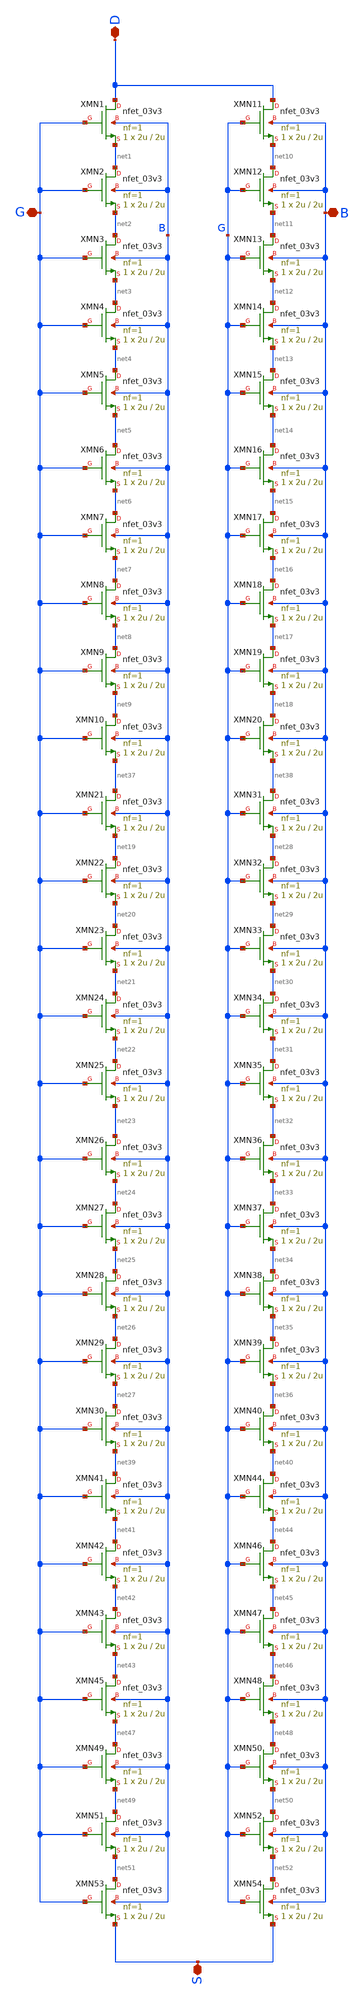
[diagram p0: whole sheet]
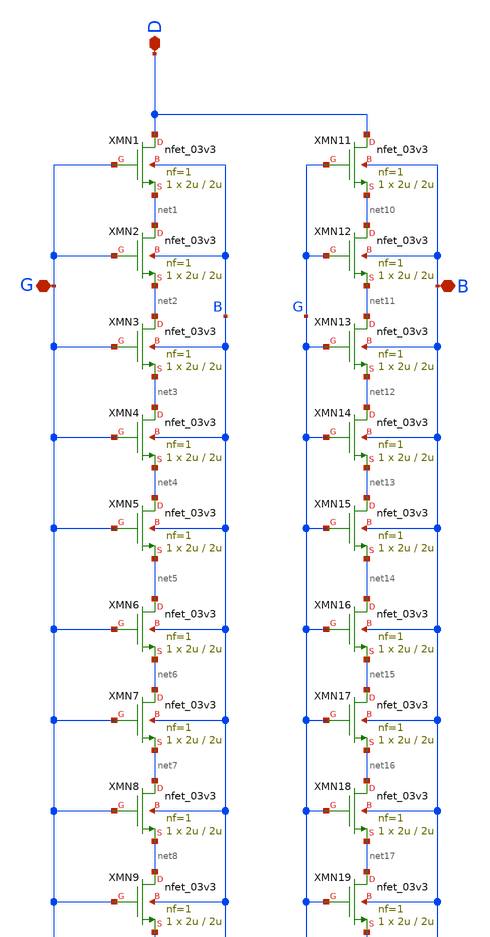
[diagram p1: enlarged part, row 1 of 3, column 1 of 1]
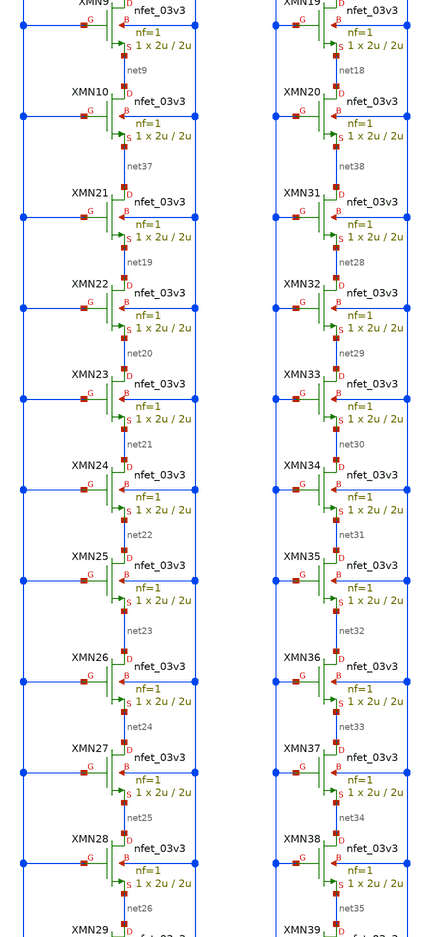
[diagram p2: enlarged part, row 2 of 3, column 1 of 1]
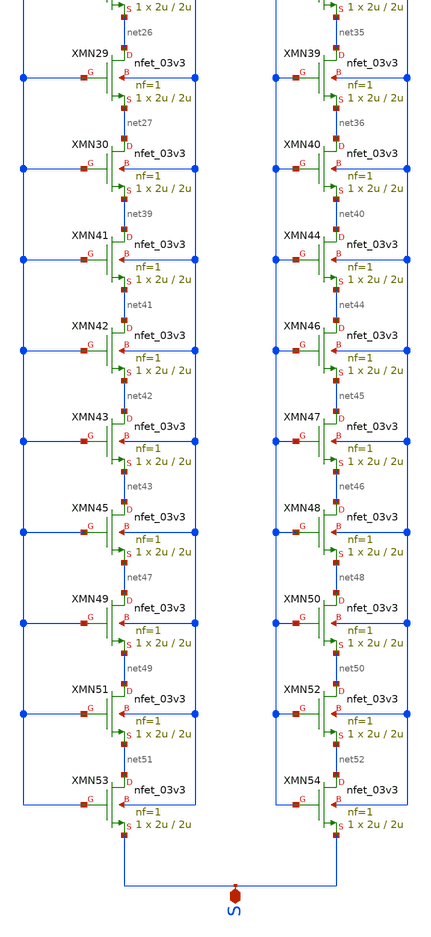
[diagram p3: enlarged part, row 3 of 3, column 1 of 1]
** sch_path: Voltage_Reference/symbols_vr/NMOS_matrix2_SCM1.sch
**.subckt NMOS_matrix2_SCM1 D G B S
*.iopin D
*.iopin G
*.iopin B
*.iopin S
XMN1 D G net1 B nfet_03v3 L=2u W=2u nf=1 ad='int((nf+1)/2) * W/nf * 0.18u' as='int((nf+2)/2) * W/nf * 0.18u'
+ pd='2*int((nf+1)/2) * (W/nf + 0.18u)' ps='2*int((nf+2)/2) * (W/nf + 0.18u)' nrd='0.18u / W' nrs='0.18u / W'
+ sa=0 sb=0 sd=0 m=1
XMN2 net1 G net2 B nfet_03v3 L=2u W=2u nf=1 ad='int((nf+1)/2) * W/nf * 0.18u' as='int((nf+2)/2) * W/nf * 0.18u'
+ pd='2*int((nf+1)/2) * (W/nf + 0.18u)' ps='2*int((nf+2)/2) * (W/nf + 0.18u)' nrd='0.18u / W' nrs='0.18u / W'
+ sa=0 sb=0 sd=0 m=1
XMN3 net2 G net3 B nfet_03v3 L=2u W=2u nf=1 ad='int((nf+1)/2) * W/nf * 0.18u' as='int((nf+2)/2) * W/nf * 0.18u'
+ pd='2*int((nf+1)/2) * (W/nf + 0.18u)' ps='2*int((nf+2)/2) * (W/nf + 0.18u)' nrd='0.18u / W' nrs='0.18u / W'
+ sa=0 sb=0 sd=0 m=1
XMN4 net3 G net4 B nfet_03v3 L=2u W=2u nf=1 ad='int((nf+1)/2) * W/nf * 0.18u' as='int((nf+2)/2) * W/nf * 0.18u'
+ pd='2*int((nf+1)/2) * (W/nf + 0.18u)' ps='2*int((nf+2)/2) * (W/nf + 0.18u)' nrd='0.18u / W' nrs='0.18u / W'
+ sa=0 sb=0 sd=0 m=1
XMN5 net4 G net5 B nfet_03v3 L=2u W=2u nf=1 ad='int((nf+1)/2) * W/nf * 0.18u' as='int((nf+2)/2) * W/nf * 0.18u'
+ pd='2*int((nf+1)/2) * (W/nf + 0.18u)' ps='2*int((nf+2)/2) * (W/nf + 0.18u)' nrd='0.18u / W' nrs='0.18u / W'
+ sa=0 sb=0 sd=0 m=1
XMN6 net5 G net6 B nfet_03v3 L=2u W=2u nf=1 ad='int((nf+1)/2) * W/nf * 0.18u' as='int((nf+2)/2) * W/nf * 0.18u'
+ pd='2*int((nf+1)/2) * (W/nf + 0.18u)' ps='2*int((nf+2)/2) * (W/nf + 0.18u)' nrd='0.18u / W' nrs='0.18u / W'
+ sa=0 sb=0 sd=0 m=1
XMN7 net6 G net7 B nfet_03v3 L=2u W=2u nf=1 ad='int((nf+1)/2) * W/nf * 0.18u' as='int((nf+2)/2) * W/nf * 0.18u'
+ pd='2*int((nf+1)/2) * (W/nf + 0.18u)' ps='2*int((nf+2)/2) * (W/nf + 0.18u)' nrd='0.18u / W' nrs='0.18u / W'
+ sa=0 sb=0 sd=0 m=1
XMN8 net7 G net8 B nfet_03v3 L=2u W=2u nf=1 ad='int((nf+1)/2) * W/nf * 0.18u' as='int((nf+2)/2) * W/nf * 0.18u'
+ pd='2*int((nf+1)/2) * (W/nf + 0.18u)' ps='2*int((nf+2)/2) * (W/nf + 0.18u)' nrd='0.18u / W' nrs='0.18u / W'
+ sa=0 sb=0 sd=0 m=1
XMN9 net8 G net9 B nfet_03v3 L=2u W=2u nf=1 ad='int((nf+1)/2) * W/nf * 0.18u' as='int((nf+2)/2) * W/nf * 0.18u'
+ pd='2*int((nf+1)/2) * (W/nf + 0.18u)' ps='2*int((nf+2)/2) * (W/nf + 0.18u)' nrd='0.18u / W' nrs='0.18u / W'
+ sa=0 sb=0 sd=0 m=1
XMN10 net9 G net37 B nfet_03v3 L=2u W=2u nf=1 ad='int((nf+1)/2) * W/nf * 0.18u' as='int((nf+2)/2) * W/nf * 0.18u'
+ pd='2*int((nf+1)/2) * (W/nf + 0.18u)' ps='2*int((nf+2)/2) * (W/nf + 0.18u)' nrd='0.18u / W' nrs='0.18u / W'
+ sa=0 sb=0 sd=0 m=1
XMN11 D G net10 B nfet_03v3 L=2u W=2u nf=1 ad='int((nf+1)/2) * W/nf * 0.18u' as='int((nf+2)/2) * W/nf * 0.18u'
+ pd='2*int((nf+1)/2) * (W/nf + 0.18u)' ps='2*int((nf+2)/2) * (W/nf + 0.18u)' nrd='0.18u / W' nrs='0.18u / W'
+ sa=0 sb=0 sd=0 m=1
XMN12 net10 G net11 B nfet_03v3 L=2u W=2u nf=1 ad='int((nf+1)/2) * W/nf * 0.18u' as='int((nf+2)/2) * W/nf * 0.18u'
+ pd='2*int((nf+1)/2) * (W/nf + 0.18u)' ps='2*int((nf+2)/2) * (W/nf + 0.18u)' nrd='0.18u / W' nrs='0.18u / W'
+ sa=0 sb=0 sd=0 m=1
XMN13 net11 G net12 B nfet_03v3 L=2u W=2u nf=1 ad='int((nf+1)/2) * W/nf * 0.18u' as='int((nf+2)/2) * W/nf * 0.18u'
+ pd='2*int((nf+1)/2) * (W/nf + 0.18u)' ps='2*int((nf+2)/2) * (W/nf + 0.18u)' nrd='0.18u / W' nrs='0.18u / W'
+ sa=0 sb=0 sd=0 m=1
XMN14 net12 G net13 B nfet_03v3 L=2u W=2u nf=1 ad='int((nf+1)/2) * W/nf * 0.18u' as='int((nf+2)/2) * W/nf * 0.18u'
+ pd='2*int((nf+1)/2) * (W/nf + 0.18u)' ps='2*int((nf+2)/2) * (W/nf + 0.18u)' nrd='0.18u / W' nrs='0.18u / W'
+ sa=0 sb=0 sd=0 m=1
XMN15 net13 G net14 B nfet_03v3 L=2u W=2u nf=1 ad='int((nf+1)/2) * W/nf * 0.18u' as='int((nf+2)/2) * W/nf * 0.18u'
+ pd='2*int((nf+1)/2) * (W/nf + 0.18u)' ps='2*int((nf+2)/2) * (W/nf + 0.18u)' nrd='0.18u / W' nrs='0.18u / W'
+ sa=0 sb=0 sd=0 m=1
XMN16 net14 G net15 B nfet_03v3 L=2u W=2u nf=1 ad='int((nf+1)/2) * W/nf * 0.18u' as='int((nf+2)/2) * W/nf * 0.18u'
+ pd='2*int((nf+1)/2) * (W/nf + 0.18u)' ps='2*int((nf+2)/2) * (W/nf + 0.18u)' nrd='0.18u / W' nrs='0.18u / W'
+ sa=0 sb=0 sd=0 m=1
XMN17 net15 G net16 B nfet_03v3 L=2u W=2u nf=1 ad='int((nf+1)/2) * W/nf * 0.18u' as='int((nf+2)/2) * W/nf * 0.18u'
+ pd='2*int((nf+1)/2) * (W/nf + 0.18u)' ps='2*int((nf+2)/2) * (W/nf + 0.18u)' nrd='0.18u / W' nrs='0.18u / W'
+ sa=0 sb=0 sd=0 m=1
XMN18 net16 G net17 B nfet_03v3 L=2u W=2u nf=1 ad='int((nf+1)/2) * W/nf * 0.18u' as='int((nf+2)/2) * W/nf * 0.18u'
+ pd='2*int((nf+1)/2) * (W/nf + 0.18u)' ps='2*int((nf+2)/2) * (W/nf + 0.18u)' nrd='0.18u / W' nrs='0.18u / W'
+ sa=0 sb=0 sd=0 m=1
XMN19 net17 G net18 B nfet_03v3 L=2u W=2u nf=1 ad='int((nf+1)/2) * W/nf * 0.18u' as='int((nf+2)/2) * W/nf * 0.18u'
+ pd='2*int((nf+1)/2) * (W/nf + 0.18u)' ps='2*int((nf+2)/2) * (W/nf + 0.18u)' nrd='0.18u / W' nrs='0.18u / W'
+ sa=0 sb=0 sd=0 m=1
XMN20 net18 G net38 B nfet_03v3 L=2u W=2u nf=1 ad='int((nf+1)/2) * W/nf * 0.18u' as='int((nf+2)/2) * W/nf * 0.18u'
+ pd='2*int((nf+1)/2) * (W/nf + 0.18u)' ps='2*int((nf+2)/2) * (W/nf + 0.18u)' nrd='0.18u / W' nrs='0.18u / W'
+ sa=0 sb=0 sd=0 m=1
XMN21 net37 G net19 B nfet_03v3 L=2u W=2u nf=1 ad='int((nf+1)/2) * W/nf * 0.18u' as='int((nf+2)/2) * W/nf * 0.18u'
+ pd='2*int((nf+1)/2) * (W/nf + 0.18u)' ps='2*int((nf+2)/2) * (W/nf + 0.18u)' nrd='0.18u / W' nrs='0.18u / W'
+ sa=0 sb=0 sd=0 m=1
XMN22 net19 G net20 B nfet_03v3 L=2u W=2u nf=1 ad='int((nf+1)/2) * W/nf * 0.18u' as='int((nf+2)/2) * W/nf * 0.18u'
+ pd='2*int((nf+1)/2) * (W/nf + 0.18u)' ps='2*int((nf+2)/2) * (W/nf + 0.18u)' nrd='0.18u / W' nrs='0.18u / W'
+ sa=0 sb=0 sd=0 m=1
XMN23 net20 G net21 B nfet_03v3 L=2u W=2u nf=1 ad='int((nf+1)/2) * W/nf * 0.18u' as='int((nf+2)/2) * W/nf * 0.18u'
+ pd='2*int((nf+1)/2) * (W/nf + 0.18u)' ps='2*int((nf+2)/2) * (W/nf + 0.18u)' nrd='0.18u / W' nrs='0.18u / W'
+ sa=0 sb=0 sd=0 m=1
XMN24 net21 G net22 B nfet_03v3 L=2u W=2u nf=1 ad='int((nf+1)/2) * W/nf * 0.18u' as='int((nf+2)/2) * W/nf * 0.18u'
+ pd='2*int((nf+1)/2) * (W/nf + 0.18u)' ps='2*int((nf+2)/2) * (W/nf + 0.18u)' nrd='0.18u / W' nrs='0.18u / W'
+ sa=0 sb=0 sd=0 m=1
XMN25 net22 G net23 B nfet_03v3 L=2u W=2u nf=1 ad='int((nf+1)/2) * W/nf * 0.18u' as='int((nf+2)/2) * W/nf * 0.18u'
+ pd='2*int((nf+1)/2) * (W/nf + 0.18u)' ps='2*int((nf+2)/2) * (W/nf + 0.18u)' nrd='0.18u / W' nrs='0.18u / W'
+ sa=0 sb=0 sd=0 m=1
XMN26 net23 G net24 B nfet_03v3 L=2u W=2u nf=1 ad='int((nf+1)/2) * W/nf * 0.18u' as='int((nf+2)/2) * W/nf * 0.18u'
+ pd='2*int((nf+1)/2) * (W/nf + 0.18u)' ps='2*int((nf+2)/2) * (W/nf + 0.18u)' nrd='0.18u / W' nrs='0.18u / W'
+ sa=0 sb=0 sd=0 m=1
XMN27 net24 G net25 B nfet_03v3 L=2u W=2u nf=1 ad='int((nf+1)/2) * W/nf * 0.18u' as='int((nf+2)/2) * W/nf * 0.18u'
+ pd='2*int((nf+1)/2) * (W/nf + 0.18u)' ps='2*int((nf+2)/2) * (W/nf + 0.18u)' nrd='0.18u / W' nrs='0.18u / W'
+ sa=0 sb=0 sd=0 m=1
XMN28 net25 G net26 B nfet_03v3 L=2u W=2u nf=1 ad='int((nf+1)/2) * W/nf * 0.18u' as='int((nf+2)/2) * W/nf * 0.18u'
+ pd='2*int((nf+1)/2) * (W/nf + 0.18u)' ps='2*int((nf+2)/2) * (W/nf + 0.18u)' nrd='0.18u / W' nrs='0.18u / W'
+ sa=0 sb=0 sd=0 m=1
XMN29 net26 G net27 B nfet_03v3 L=2u W=2u nf=1 ad='int((nf+1)/2) * W/nf * 0.18u' as='int((nf+2)/2) * W/nf * 0.18u'
+ pd='2*int((nf+1)/2) * (W/nf + 0.18u)' ps='2*int((nf+2)/2) * (W/nf + 0.18u)' nrd='0.18u / W' nrs='0.18u / W'
+ sa=0 sb=0 sd=0 m=1
XMN30 net27 G net39 B nfet_03v3 L=2u W=2u nf=1 ad='int((nf+1)/2) * W/nf * 0.18u' as='int((nf+2)/2) * W/nf * 0.18u'
+ pd='2*int((nf+1)/2) * (W/nf + 0.18u)' ps='2*int((nf+2)/2) * (W/nf + 0.18u)' nrd='0.18u / W' nrs='0.18u / W'
+ sa=0 sb=0 sd=0 m=1
XMN31 net38 G net28 B nfet_03v3 L=2u W=2u nf=1 ad='int((nf+1)/2) * W/nf * 0.18u' as='int((nf+2)/2) * W/nf * 0.18u'
+ pd='2*int((nf+1)/2) * (W/nf + 0.18u)' ps='2*int((nf+2)/2) * (W/nf + 0.18u)' nrd='0.18u / W' nrs='0.18u / W'
+ sa=0 sb=0 sd=0 m=1
XMN32 net28 G net29 B nfet_03v3 L=2u W=2u nf=1 ad='int((nf+1)/2) * W/nf * 0.18u' as='int((nf+2)/2) * W/nf * 0.18u'
+ pd='2*int((nf+1)/2) * (W/nf + 0.18u)' ps='2*int((nf+2)/2) * (W/nf + 0.18u)' nrd='0.18u / W' nrs='0.18u / W'
+ sa=0 sb=0 sd=0 m=1
XMN33 net29 G net30 B nfet_03v3 L=2u W=2u nf=1 ad='int((nf+1)/2) * W/nf * 0.18u' as='int((nf+2)/2) * W/nf * 0.18u'
+ pd='2*int((nf+1)/2) * (W/nf + 0.18u)' ps='2*int((nf+2)/2) * (W/nf + 0.18u)' nrd='0.18u / W' nrs='0.18u / W'
+ sa=0 sb=0 sd=0 m=1
XMN34 net30 G net31 B nfet_03v3 L=2u W=2u nf=1 ad='int((nf+1)/2) * W/nf * 0.18u' as='int((nf+2)/2) * W/nf * 0.18u'
+ pd='2*int((nf+1)/2) * (W/nf + 0.18u)' ps='2*int((nf+2)/2) * (W/nf + 0.18u)' nrd='0.18u / W' nrs='0.18u / W'
+ sa=0 sb=0 sd=0 m=1
XMN35 net31 G net32 B nfet_03v3 L=2u W=2u nf=1 ad='int((nf+1)/2) * W/nf * 0.18u' as='int((nf+2)/2) * W/nf * 0.18u'
+ pd='2*int((nf+1)/2) * (W/nf + 0.18u)' ps='2*int((nf+2)/2) * (W/nf + 0.18u)' nrd='0.18u / W' nrs='0.18u / W'
+ sa=0 sb=0 sd=0 m=1
XMN36 net32 G net33 B nfet_03v3 L=2u W=2u nf=1 ad='int((nf+1)/2) * W/nf * 0.18u' as='int((nf+2)/2) * W/nf * 0.18u'
+ pd='2*int((nf+1)/2) * (W/nf + 0.18u)' ps='2*int((nf+2)/2) * (W/nf + 0.18u)' nrd='0.18u / W' nrs='0.18u / W'
+ sa=0 sb=0 sd=0 m=1
XMN37 net33 G net34 B nfet_03v3 L=2u W=2u nf=1 ad='int((nf+1)/2) * W/nf * 0.18u' as='int((nf+2)/2) * W/nf * 0.18u'
+ pd='2*int((nf+1)/2) * (W/nf + 0.18u)' ps='2*int((nf+2)/2) * (W/nf + 0.18u)' nrd='0.18u / W' nrs='0.18u / W'
+ sa=0 sb=0 sd=0 m=1
XMN38 net34 G net35 B nfet_03v3 L=2u W=2u nf=1 ad='int((nf+1)/2) * W/nf * 0.18u' as='int((nf+2)/2) * W/nf * 0.18u'
+ pd='2*int((nf+1)/2) * (W/nf + 0.18u)' ps='2*int((nf+2)/2) * (W/nf + 0.18u)' nrd='0.18u / W' nrs='0.18u / W'
+ sa=0 sb=0 sd=0 m=1
XMN39 net35 G net36 B nfet_03v3 L=2u W=2u nf=1 ad='int((nf+1)/2) * W/nf * 0.18u' as='int((nf+2)/2) * W/nf * 0.18u'
+ pd='2*int((nf+1)/2) * (W/nf + 0.18u)' ps='2*int((nf+2)/2) * (W/nf + 0.18u)' nrd='0.18u / W' nrs='0.18u / W'
+ sa=0 sb=0 sd=0 m=1
XMN40 net36 G net40 B nfet_03v3 L=2u W=2u nf=1 ad='int((nf+1)/2) * W/nf * 0.18u' as='int((nf+2)/2) * W/nf * 0.18u'
+ pd='2*int((nf+1)/2) * (W/nf + 0.18u)' ps='2*int((nf+2)/2) * (W/nf + 0.18u)' nrd='0.18u / W' nrs='0.18u / W'
+ sa=0 sb=0 sd=0 m=1
XMN41 net39 G net41 B nfet_03v3 L=2u W=2u nf=1 ad='int((nf+1)/2) * W/nf * 0.18u' as='int((nf+2)/2) * W/nf * 0.18u'
+ pd='2*int((nf+1)/2) * (W/nf + 0.18u)' ps='2*int((nf+2)/2) * (W/nf + 0.18u)' nrd='0.18u / W' nrs='0.18u / W'
+ sa=0 sb=0 sd=0 m=1
XMN44 net40 G net44 B nfet_03v3 L=2u W=2u nf=1 ad='int((nf+1)/2) * W/nf * 0.18u' as='int((nf+2)/2) * W/nf * 0.18u'
+ pd='2*int((nf+1)/2) * (W/nf + 0.18u)' ps='2*int((nf+2)/2) * (W/nf + 0.18u)' nrd='0.18u / W' nrs='0.18u / W'
+ sa=0 sb=0 sd=0 m=1
XMN42 net41 G net42 B nfet_03v3 L=2u W=2u nf=1 ad='int((nf+1)/2) * W/nf * 0.18u' as='int((nf+2)/2) * W/nf * 0.18u'
+ pd='2*int((nf+1)/2) * (W/nf + 0.18u)' ps='2*int((nf+2)/2) * (W/nf + 0.18u)' nrd='0.18u / W' nrs='0.18u / W'
+ sa=0 sb=0 sd=0 m=1
XMN43 net42 G net43 B nfet_03v3 L=2u W=2u nf=1 ad='int((nf+1)/2) * W/nf * 0.18u' as='int((nf+2)/2) * W/nf * 0.18u'
+ pd='2*int((nf+1)/2) * (W/nf + 0.18u)' ps='2*int((nf+2)/2) * (W/nf + 0.18u)' nrd='0.18u / W' nrs='0.18u / W'
+ sa=0 sb=0 sd=0 m=1
XMN45 net43 G net47 B nfet_03v3 L=2u W=2u nf=1 ad='int((nf+1)/2) * W/nf * 0.18u' as='int((nf+2)/2) * W/nf * 0.18u'
+ pd='2*int((nf+1)/2) * (W/nf + 0.18u)' ps='2*int((nf+2)/2) * (W/nf + 0.18u)' nrd='0.18u / W' nrs='0.18u / W'
+ sa=0 sb=0 sd=0 m=1
XMN46 net44 G net45 B nfet_03v3 L=2u W=2u nf=1 ad='int((nf+1)/2) * W/nf * 0.18u' as='int((nf+2)/2) * W/nf * 0.18u'
+ pd='2*int((nf+1)/2) * (W/nf + 0.18u)' ps='2*int((nf+2)/2) * (W/nf + 0.18u)' nrd='0.18u / W' nrs='0.18u / W'
+ sa=0 sb=0 sd=0 m=1
XMN47 net45 G net46 B nfet_03v3 L=2u W=2u nf=1 ad='int((nf+1)/2) * W/nf * 0.18u' as='int((nf+2)/2) * W/nf * 0.18u'
+ pd='2*int((nf+1)/2) * (W/nf + 0.18u)' ps='2*int((nf+2)/2) * (W/nf + 0.18u)' nrd='0.18u / W' nrs='0.18u / W'
+ sa=0 sb=0 sd=0 m=1
XMN48 net46 G net48 B nfet_03v3 L=2u W=2u nf=1 ad='int((nf+1)/2) * W/nf * 0.18u' as='int((nf+2)/2) * W/nf * 0.18u'
+ pd='2*int((nf+1)/2) * (W/nf + 0.18u)' ps='2*int((nf+2)/2) * (W/nf + 0.18u)' nrd='0.18u / W' nrs='0.18u / W'
+ sa=0 sb=0 sd=0 m=1
XMN49 net47 G net49 B nfet_03v3 L=2u W=2u nf=1 ad='int((nf+1)/2) * W/nf * 0.18u' as='int((nf+2)/2) * W/nf * 0.18u'
+ pd='2*int((nf+1)/2) * (W/nf + 0.18u)' ps='2*int((nf+2)/2) * (W/nf + 0.18u)' nrd='0.18u / W' nrs='0.18u / W'
+ sa=0 sb=0 sd=0 m=1
XMN50 net48 G net50 B nfet_03v3 L=2u W=2u nf=1 ad='int((nf+1)/2) * W/nf * 0.18u' as='int((nf+2)/2) * W/nf * 0.18u'
+ pd='2*int((nf+1)/2) * (W/nf + 0.18u)' ps='2*int((nf+2)/2) * (W/nf + 0.18u)' nrd='0.18u / W' nrs='0.18u / W'
+ sa=0 sb=0 sd=0 m=1
XMN51 net49 G net51 B nfet_03v3 L=2u W=2u nf=1 ad='int((nf+1)/2) * W/nf * 0.18u' as='int((nf+2)/2) * W/nf * 0.18u'
+ pd='2*int((nf+1)/2) * (W/nf + 0.18u)' ps='2*int((nf+2)/2) * (W/nf + 0.18u)' nrd='0.18u / W' nrs='0.18u / W'
+ sa=0 sb=0 sd=0 m=1
XMN52 net50 G net52 B nfet_03v3 L=2u W=2u nf=1 ad='int((nf+1)/2) * W/nf * 0.18u' as='int((nf+2)/2) * W/nf * 0.18u'
+ pd='2*int((nf+1)/2) * (W/nf + 0.18u)' ps='2*int((nf+2)/2) * (W/nf + 0.18u)' nrd='0.18u / W' nrs='0.18u / W'
+ sa=0 sb=0 sd=0 m=1
XMN53 net51 G S B nfet_03v3 L=2u W=2u nf=1 ad='int((nf+1)/2) * W/nf * 0.18u' as='int((nf+2)/2) * W/nf * 0.18u'
+ pd='2*int((nf+1)/2) * (W/nf + 0.18u)' ps='2*int((nf+2)/2) * (W/nf + 0.18u)' nrd='0.18u / W' nrs='0.18u / W'
+ sa=0 sb=0 sd=0 m=1
XMN54 net52 G S B nfet_03v3 L=2u W=2u nf=1 ad='int((nf+1)/2) * W/nf * 0.18u' as='int((nf+2)/2) * W/nf * 0.18u'
+ pd='2*int((nf+1)/2) * (W/nf + 0.18u)' ps='2*int((nf+2)/2) * (W/nf + 0.18u)' nrd='0.18u / W' nrs='0.18u / W'
+ sa=0 sb=0 sd=0 m=1
**.ends
.end
